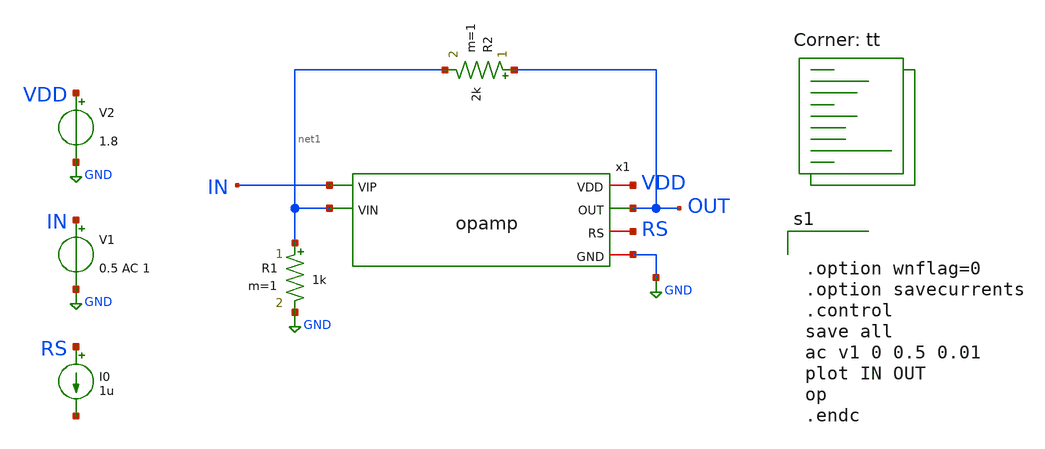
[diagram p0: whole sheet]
** sch_path: OPAMP/xschem/opamp_tb.sch
**.subckt opamp_tb
V1 IN GND 0.5 AC 1
V2 VDD GND 1.8
R1 net1 GND 1k m=1
R2 OUT net1 2k m=1
x1 VDD IN net1 OUT RS GND opamp
I0 RS net2 1u
**** begin user architecture code
.lib $::SKYWATER_MODELS/sky130.lib.spice tt


.option wnflag=0
.option savecurrents
.control
save all
ac v1 0 0.5 0.01
plot IN OUT
op
.endc


**** end user architecture code
**.ends

* expanding   symbol:  opamp.sym # of pins=6
** sym_path: OPAMP/xschem/opamp.sym
** sch_path: OPAMP/xschem/opamp.sch
.subckt opamp VDD VIP VIN OUT RS GND
*.iopin GND
*.iopin VDD
*.iopin RS
*.ipin VIN
*.ipin VIP
*.opin OUT
XM3 net2 net2 GND GND sky130_fd_pr__nfet_01v8 L=1u W=2u nf=1 ad='int((nf+1)/2) * W/nf * 0.29' as='int((nf+2)/2) * W/nf * 0.29'
+ pd='2*int((nf+1)/2) * (W/nf + 0.29)' ps='2*int((nf+2)/2) * (W/nf + 0.29)' nrd='0.29 / W' nrs='0.29 / W'
+ sa=0 sb=0 sd=0 mult=2 m=2
XM4 net1 net2 RS GND sky130_fd_pr__nfet_01v8 L=1u W=2u nf=1 ad='int((nf+1)/2) * W/nf * 0.29' as='int((nf+2)/2) * W/nf * 0.29'
+ pd='2*int((nf+1)/2) * (W/nf + 0.29)' ps='2*int((nf+2)/2) * (W/nf + 0.29)' nrd='0.29 / W' nrs='0.29 / W'
+ sa=0 sb=0 sd=0 mult=2 m=2
XM2 net1 net1 VDD VDD sky130_fd_pr__pfet_01v8 L=1u W=2u nf=1 ad='int((nf+1)/2) * W/nf * 0.29' as='int((nf+2)/2) * W/nf * 0.29'
+ pd='2*int((nf+1)/2) * (W/nf + 0.29)' ps='2*int((nf+2)/2) * (W/nf + 0.29)' nrd='0.29 / W' nrs='0.29 / W'
+ sa=0 sb=0 sd=0 mult=2 m=2
XM1 net2 net1 VDD VDD sky130_fd_pr__pfet_01v8 L=1u W=2u nf=1 ad='int((nf+1)/2) * W/nf * 0.29' as='int((nf+2)/2) * W/nf * 0.29'
+ pd='2*int((nf+1)/2) * (W/nf + 0.29)' ps='2*int((nf+2)/2) * (W/nf + 0.29)' nrd='0.29 / W' nrs='0.29 / W'
+ sa=0 sb=0 sd=0 mult=2 m=2
XM5 net3 net1 VDD VDD sky130_fd_pr__pfet_01v8 L=1u W=2u nf=1 ad='int((nf+1)/2) * W/nf * 0.29' as='int((nf+2)/2) * W/nf * 0.29'
+ pd='2*int((nf+1)/2) * (W/nf + 0.29)' ps='2*int((nf+2)/2) * (W/nf + 0.29)' nrd='0.29 / W' nrs='0.29 / W'
+ sa=0 sb=0 sd=0 mult=2 m=2
XM6 net4 VIN net3 VDD sky130_fd_pr__pfet_01v8 L=0.5 W=1 nf=1 ad='int((nf+1)/2) * W/nf * 0.29' as='int((nf+2)/2) * W/nf * 0.29'
+ pd='2*int((nf+1)/2) * (W/nf + 0.29)' ps='2*int((nf+2)/2) * (W/nf + 0.29)' nrd='0.29 / W' nrs='0.29 / W'
+ sa=0 sb=0 sd=0 mult=4 m=4
XM7 OUT VIP net3 VDD sky130_fd_pr__pfet_01v8 L=0.5 W=1 nf=1 ad='int((nf+1)/2) * W/nf * 0.29' as='int((nf+2)/2) * W/nf * 0.29'
+ pd='2*int((nf+1)/2) * (W/nf + 0.29)' ps='2*int((nf+2)/2) * (W/nf + 0.29)' nrd='0.29 / W' nrs='0.29 / W'
+ sa=0 sb=0 sd=0 mult=4 m=4
XM8 net4 net4 GND GND sky130_fd_pr__nfet_01v8 L=0.8 W=1 nf=1 ad='int((nf+1)/2) * W/nf * 0.29' as='int((nf+2)/2) * W/nf * 0.29'
+ pd='2*int((nf+1)/2) * (W/nf + 0.29)' ps='2*int((nf+2)/2) * (W/nf + 0.29)' nrd='0.29 / W' nrs='0.29 / W'
+ sa=0 sb=0 sd=0 mult=4 m=4
XM9 OUT net4 GND GND sky130_fd_pr__nfet_01v8 L=0.8 W=1 nf=1 ad='int((nf+1)/2) * W/nf * 0.29' as='int((nf+2)/2) * W/nf * 0.29'
+ pd='2*int((nf+1)/2) * (W/nf + 0.29)' ps='2*int((nf+2)/2) * (W/nf + 0.29)' nrd='0.29 / W' nrs='0.29 / W'
+ sa=0 sb=0 sd=0 mult=4 m=4
.ends

.GLOBAL GND
.end
